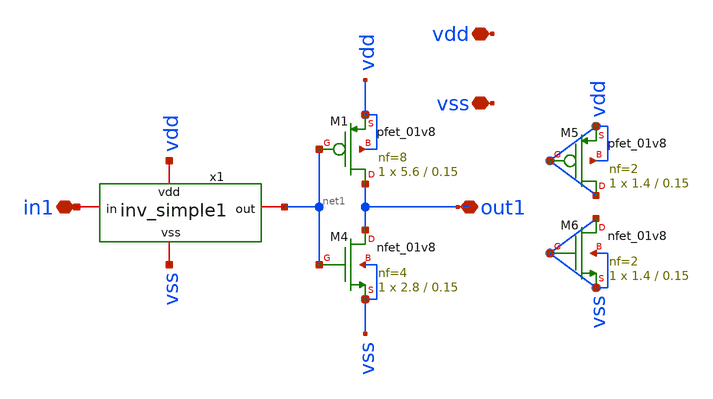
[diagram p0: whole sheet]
** sch_path: xschem/inv_buffer2.sch
**.subckt inv_buffer2 in1 out1 vdd vss
*.iopin in1
*.iopin out1
*.iopin vdd
*.iopin vss
XM4 out1 net1 vss vss sky130_fd_pr__nfet_01v8 L=0.15 W=2.8 nf=4 ad='int((nf+1)/2) * W/nf * 0.29' as='int((nf+2)/2) * W/nf * 0.29'
+ pd='2*int((nf+1)/2) * (W/nf + 0.29)' ps='2*int((nf+2)/2) * (W/nf + 0.29)' nrd='0.29 / W' nrs='0.29 / W'
+ sa=0 sb=0 sd=0 mult=1 m=1
XM1 out1 net1 vdd vdd sky130_fd_pr__pfet_01v8 L=0.15 W=5.6 nf=8 ad='int((nf+1)/2) * W/nf * 0.29' as='int((nf+2)/2) * W/nf * 0.29'
+ pd='2*int((nf+1)/2) * (W/nf + 0.29)' ps='2*int((nf+2)/2) * (W/nf + 0.29)' nrd='0.29 / W' nrs='0.29 / W'
+ sa=0 sb=0 sd=0 mult=1 m=1
XM5 vdd vdd vdd vdd sky130_fd_pr__pfet_01v8 L=0.15 W=1.4 nf=2 ad='int((nf+1)/2) * W/nf * 0.29' as='int((nf+2)/2) * W/nf * 0.29'
+ pd='2*int((nf+1)/2) * (W/nf + 0.29)' ps='2*int((nf+2)/2) * (W/nf + 0.29)' nrd='0.29 / W' nrs='0.29 / W'
+ sa=0 sb=0 sd=0 mult=1 m=1
XM6 vss vss vss vss sky130_fd_pr__nfet_01v8 L=0.15 W=1.4 nf=2 ad='int((nf+1)/2) * W/nf * 0.29' as='int((nf+2)/2) * W/nf * 0.29'
+ pd='2*int((nf+1)/2) * (W/nf + 0.29)' ps='2*int((nf+2)/2) * (W/nf + 0.29)' nrd='0.29 / W' nrs='0.29 / W'
+ sa=0 sb=0 sd=0 mult=1 m=1
x1 vdd in1 net1 vss inv_simple1
**.ends

* expanding   symbol:  inv_simple1.sym # of pins=4
** sym_path: xschem/inv_simple1.sym
** sch_path: xschem/inv_simple1.sch
.subckt inv_simple1 vdd in out vss
*.iopin in
*.iopin vdd
*.iopin vss
*.iopin out
XM19 out in vss vss sky130_fd_pr__nfet_01v8 L=0.15 W=1.4 nf=1 ad='int((nf+1)/2) * W/nf * 0.29' as='int((nf+2)/2) * W/nf * 0.29'
+ pd='2*int((nf+1)/2) * (W/nf + 0.29)' ps='2*int((nf+2)/2) * (W/nf + 0.29)' nrd='0.29 / W' nrs='0.29 / W'
+ sa=0 sb=0 sd=0 mult=1 m=1
XM20 out in vdd vdd sky130_fd_pr__pfet_01v8 L=0.15 W=2.8 nf=1 ad='int((nf+1)/2) * W/nf * 0.29' as='int((nf+2)/2) * W/nf * 0.29'
+ pd='2*int((nf+1)/2) * (W/nf + 0.29)' ps='2*int((nf+2)/2) * (W/nf + 0.29)' nrd='0.29 / W' nrs='0.29 / W'
+ sa=0 sb=0 sd=0 mult=1 m=1
XM1 vdd vdd vdd vdd sky130_fd_pr__pfet_01v8 L=0.15 W=1.4 nf=1 ad='int((nf+1)/2) * W/nf * 0.29' as='int((nf+2)/2) * W/nf * 0.29'
+ pd='2*int((nf+1)/2) * (W/nf + 0.29)' ps='2*int((nf+2)/2) * (W/nf + 0.29)' nrd='0.29 / W' nrs='0.29 / W'
+ sa=0 sb=0 sd=0 mult=1 m=1
XM2 vss vss vss vss sky130_fd_pr__nfet_01v8 L=0.15 W=1.4 nf=1 ad='int((nf+1)/2) * W/nf * 0.29' as='int((nf+2)/2) * W/nf * 0.29'
+ pd='2*int((nf+1)/2) * (W/nf + 0.29)' ps='2*int((nf+2)/2) * (W/nf + 0.29)' nrd='0.29 / W' nrs='0.29 / W'
+ sa=0 sb=0 sd=0 mult=1 m=1
.ends

.end
